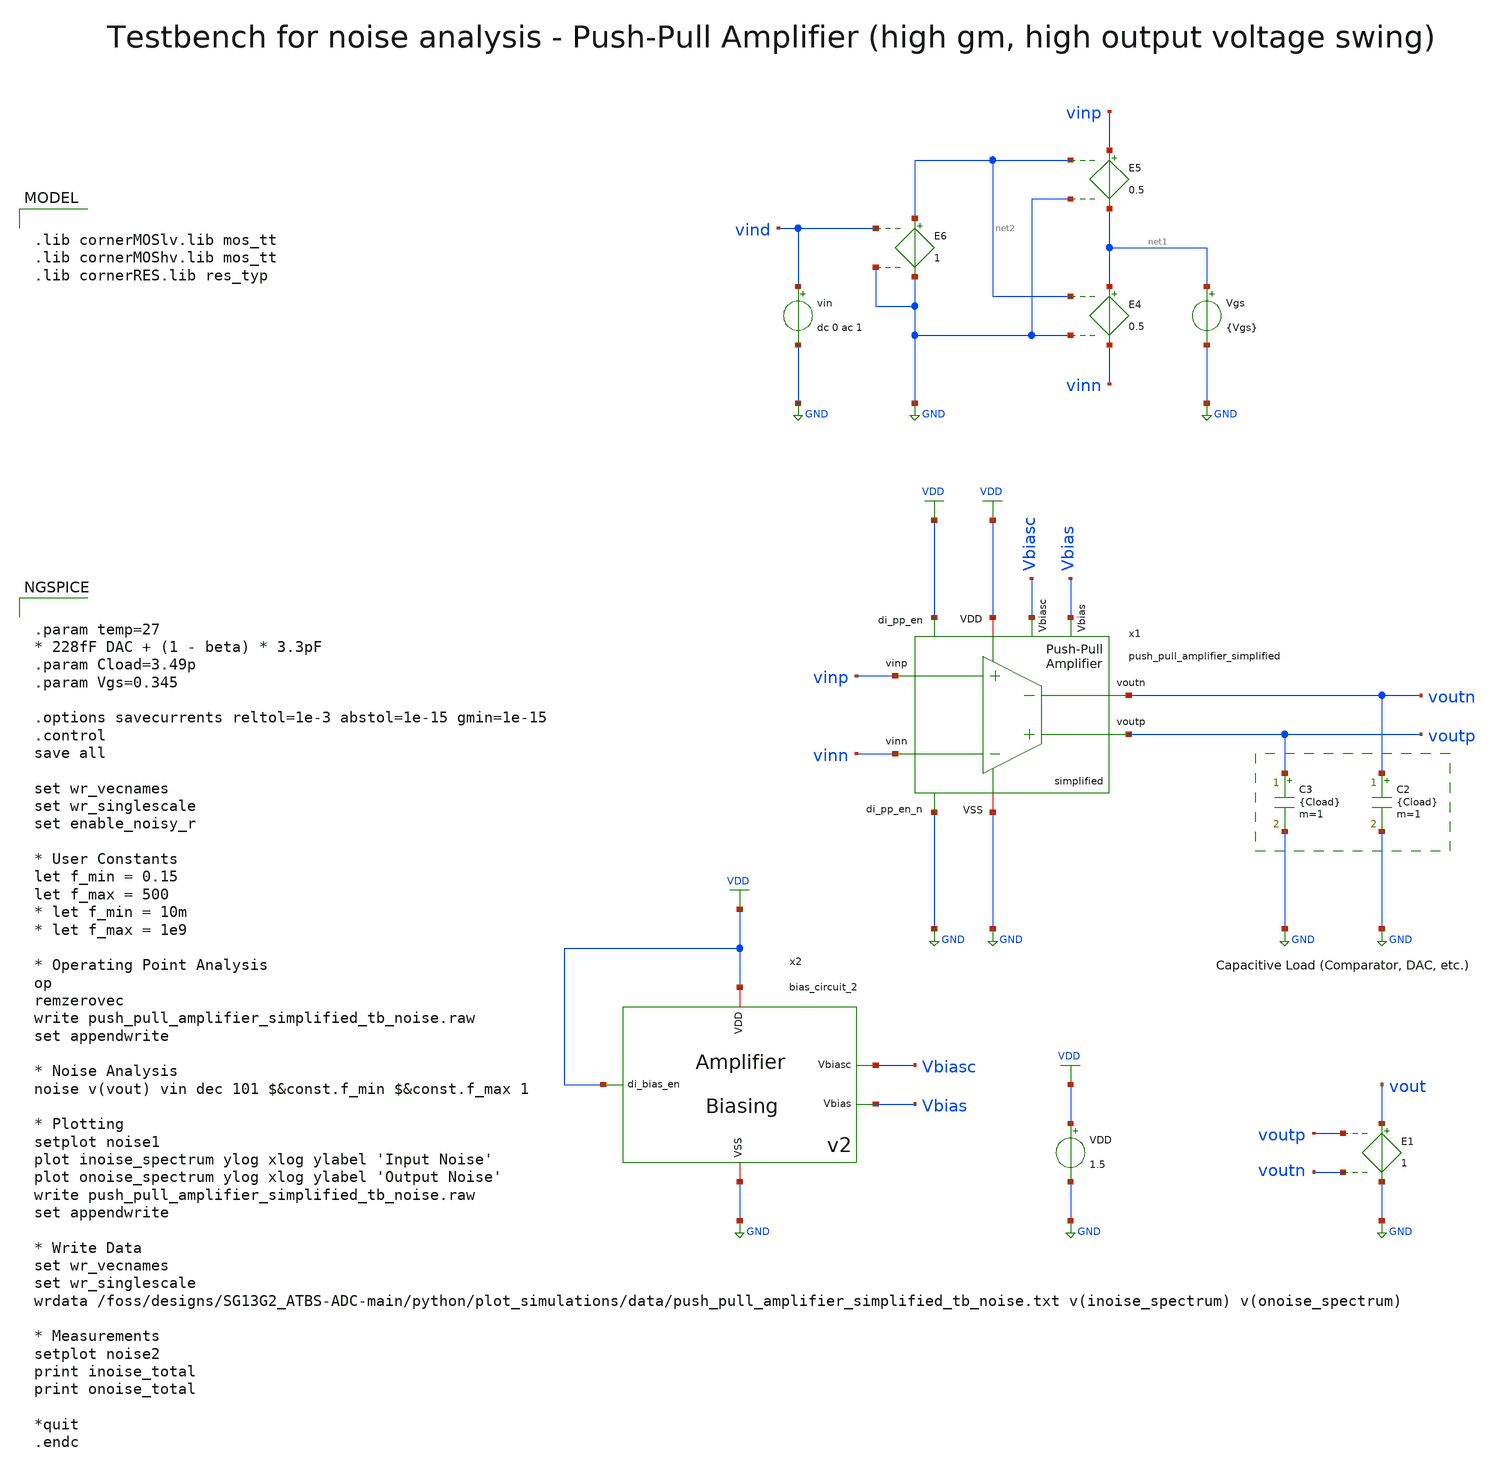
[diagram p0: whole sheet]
** sch_path: SG13G2_ATBS-ADC-main/xschem/bio_amplifier/amplifier_core/push_pull_amplifier/testbenches/push_pull_amplifier_simplified_tb_noise.sch
**.subckt push_pull_amplifier_simplified_tb_noise
VDD VDD GND 1.5
Vgs net1 GND {Vgs}
E4 net1 vinn net2 GND 0.5
E5 vinp net1 net2 GND 0.5
E6 net2 GND vind GND 1
vin vind GND dc 0 ac 1
C2 voutn GND {Cload} m=1
C3 voutp GND {Cload} m=1
E1 vout GND voutp voutn 1
x1 VDD voutp voutn vinn vinp GND GND VDD Vbiasc Vbias push_pull_amplifier_simplified
x2 VDD Vbiasc VDD GND Vbias bias_circuit_2
**** begin user architecture code


.param temp=27
* 228fF DAC + (1 - beta) * 3.3pF
.param Cload=3.49p
.param Vgs=0.345

.options savecurrents reltol=1e-3 abstol=1e-15 gmin=1e-15
.control
save all

set wr_vecnames
set wr_singlescale
set enable_noisy_r

* User Constants
let f_min = 0.15
let f_max = 500
* let f_min = 10m
* let f_max = 1e9

* Operating Point Analysis
op
remzerovec
write push_pull_amplifier_simplified_tb_noise.raw
set appendwrite

* Noise Analysis
noise v(vout) vin dec 101 $&const.f_min $&const.f_max 1

* Plotting
setplot noise1
plot inoise_spectrum ylog xlog ylabel 'Input Noise'
plot onoise_spectrum ylog xlog ylabel 'Output Noise'
write push_pull_amplifier_simplified_tb_noise.raw
set appendwrite

* Write Data
set wr_vecnames
set wr_singlescale
wrdata
+ /foss/designs/SG13G2_ATBS-ADC-main/python/plot_simulations/data/push_pull_amplifier_simplified_tb_noise.txt v(inoise_spectrum) v(onoise_spectrum)

* Measurements
setplot noise2
print inoise_total
print onoise_total

*quit
.endc



.lib cornerMOSlv.lib mos_tt
.lib cornerMOShv.lib mos_tt
.lib cornerRES.lib res_typ

**** end user architecture code
**.ends
.GLOBAL GND
.GLOBAL VDD
.end
